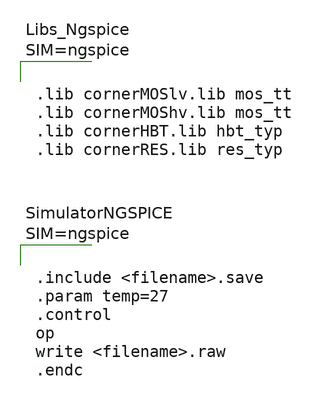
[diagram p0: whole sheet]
** sch_path: Schematics/OTA/ota_n.sch
**.subckt ota_n
**** begin user architecture code



.lib cornerMOSlv.lib mos_tt
.lib cornerMOShv.lib mos_tt
.lib cornerHBT.lib hbt_typ
.lib cornerRES.lib res_typ






.include <filename>.save
.param temp=27
.control
op
write <filename>.raw
.endc



**** end user architecture code
**.ends
.end
